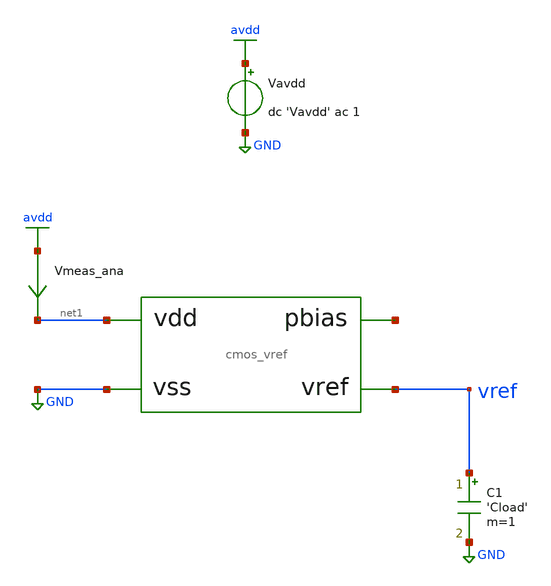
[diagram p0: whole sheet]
** sch_path: tb/cmos_vref/tb_vref_noise.sch
**.subckt tb_vref_noise
Vavdd avdd GND dc 'Vavdd' ac 1
C1 vref GND 'Cload' m=1
Vmeas_ana avdd net1 0
.save i(vmeas_ana)
X1 vref net1 GND net2 cmos_vref
**** begin user architecture code


.lib 'models_dir'/cornerMOShv.lib 'mos_corner'
.lib 'models_dir'/cornerMOSlv.lib 'mos_corner'
.lib 'models_dir'/cornerCAP.lib cap_typ
.preprocess replaceground true
.option temp='temperature'
.op
.noise v(vref) Vavdd dec 20 'frequency_start' 'frequency_stop'
.print noise file='simpath'/'filename'_'N'.data ONOISE


**** end user architecture code
**.ends
.GLOBAL avdd
.GLOBAL GND
.end
